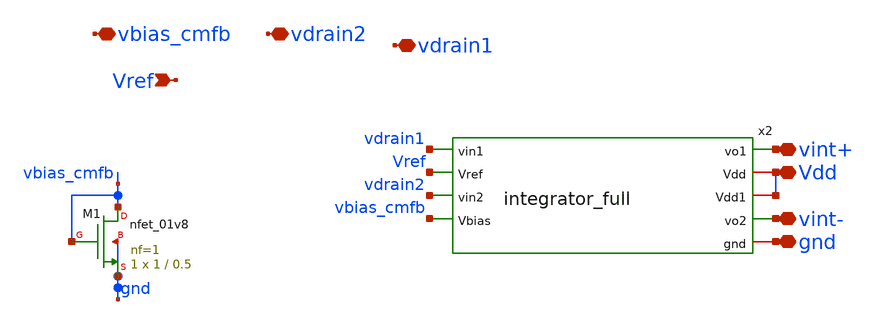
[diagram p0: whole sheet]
** sch_path: xschem/open_loop.sch
**.subckt open_loop gnd Vdd Vref vbias_cmfb vint+ vint- vdrain2 vdrain1
*.iopin gnd
*.iopin Vdd
*.ipin Vref
*.iopin vbias_cmfb
*.iopin vint+
*.iopin vint-
*.iopin vdrain2
*.iopin vdrain1
x2 vint+ Vdd Vdd vint- gnd vdrain1 Vref vdrain2 vbias_cmfb integrator_full
XM1 vbias_cmfb vbias_cmfb gnd gnd sky130_fd_pr__nfet_01v8 L=0.5 W=1 nf=1 ad='int((nf+1)/2) * W/nf * 0.29'
+ as='int((nf+2)/2) * W/nf * 0.29' pd='2*int((nf+1)/2) * (W/nf + 0.29)' ps='2*int((nf+2)/2) * (W/nf + 0.29)'
+ nrd='0.29 / W' nrs='0.29 / W' sa=0 sb=0 sd=0 mult=1 m=1
**.ends
.end
